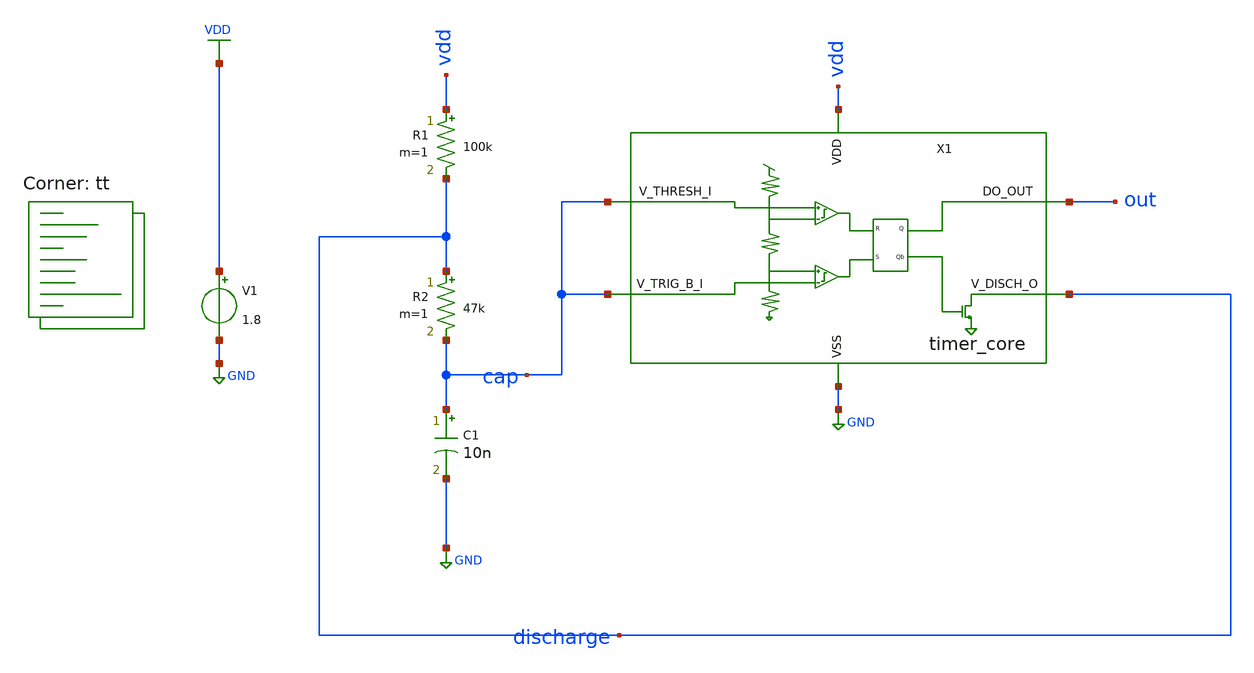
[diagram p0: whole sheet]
** sch_path: xsch/tb/tb_timer_core_astable.sch
**.subckt tb_timer_core_astable
V1 VDD GND 1.8
X1 vdd out GND discharge cap cap timer_core
R1 vdd discharge 100k m=1
R2 discharge cap 47k m=1
C1 cap GND 10n m=1
**** begin user architecture code


.tran 0.01u 10m


.lib $::SKYWATER_MODELS/sky130.lib.spice tt


.save all


**** end user architecture code
**.ends
.GLOBAL VDD
.GLOBAL GND
.end
